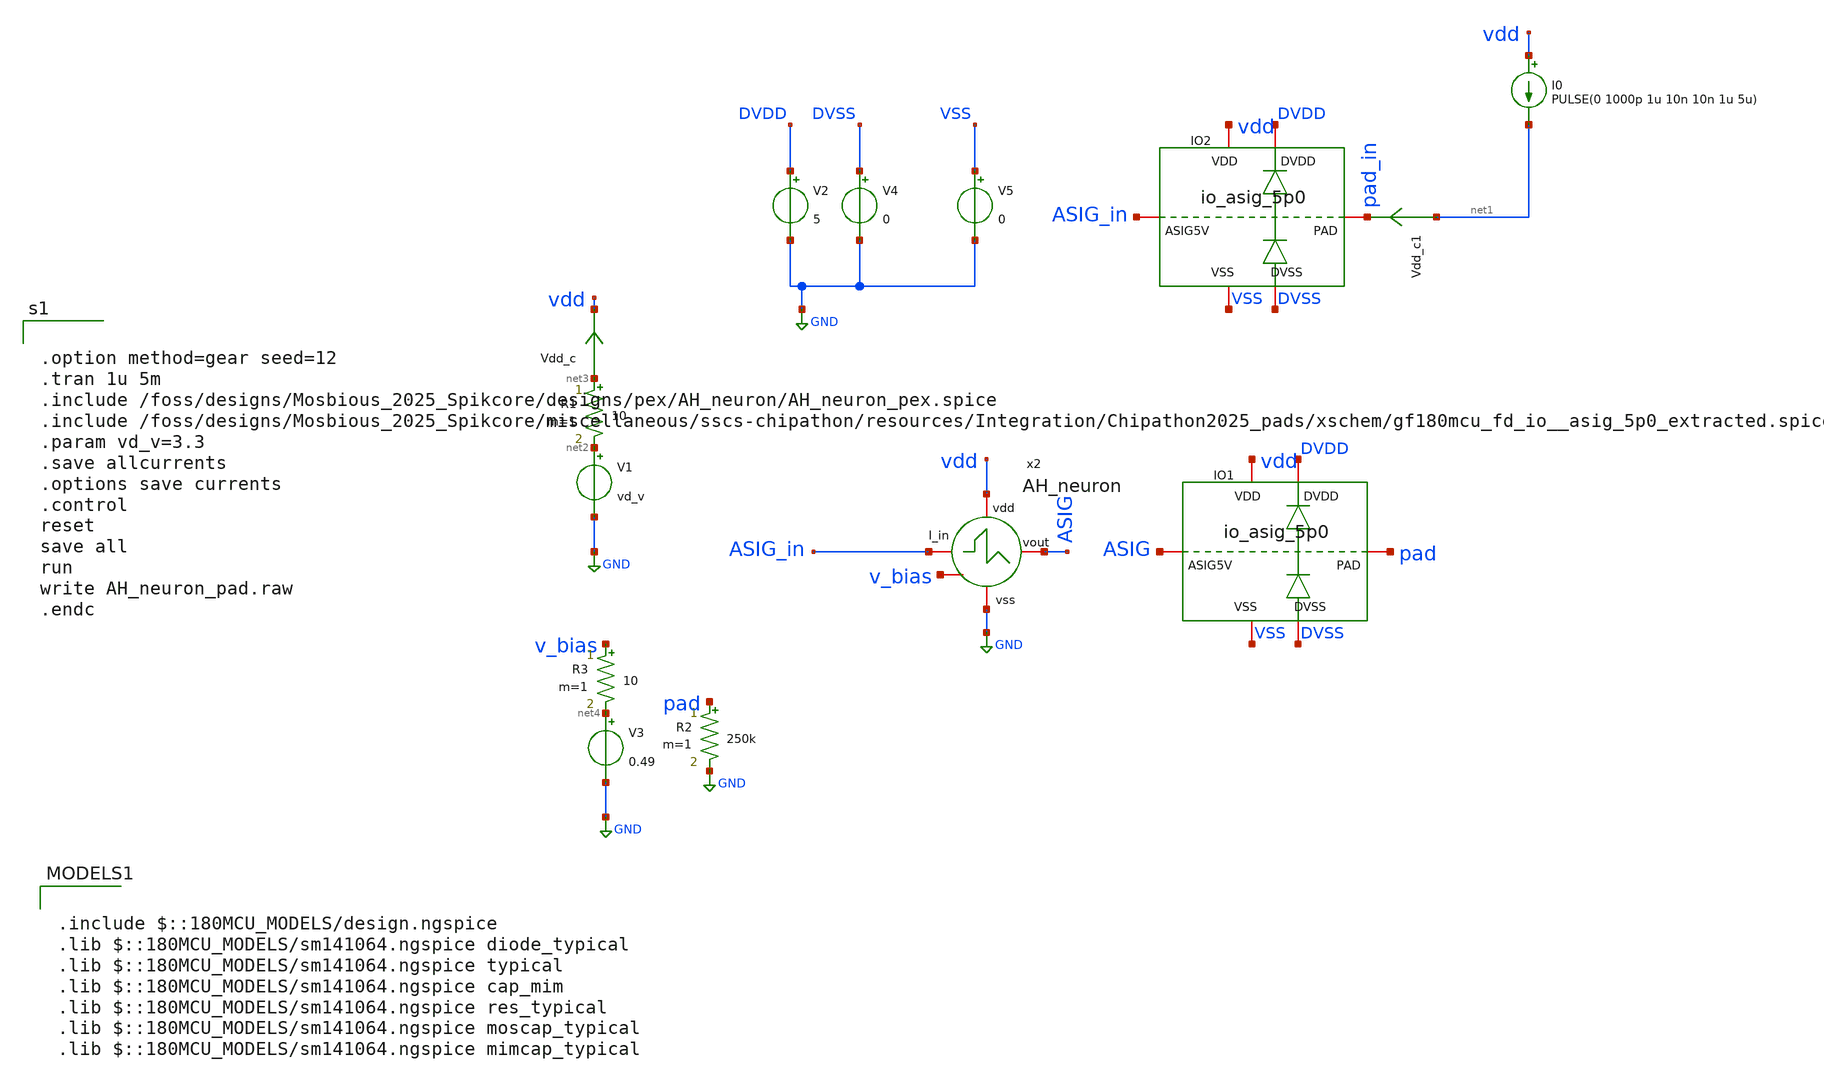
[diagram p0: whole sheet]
** sch_path: designs/libs/tb_core_analogs_pads/tb_AH_neuron/AH_neuron.sch
**.subckt AH_neuron
V1 net2 GND vd_v
Vdd_c net3 vdd 0
.save i(vdd_c)
I0 vdd net1 PULSE(0 1000p 1u 10n 10n 1u 5u)
R1 net3 net2 10 m=1
R2 pad GND 250k m=1
Vdd_c1 net1 pad_in 0
.save i(vdd_c1)
V2 DVDD GND 5
V4 DVSS GND 0
V5 VSS GND 0
XIO1 DVSS DVDD VSS vdd pad ASIG gf180mcu_fd_io__asig_5p0_extracted
V3 net4 GND 0.49
R3 v_bias net4 10 m=1
XIO2 DVSS DVDD VSS vdd pad_in ASIG_in gf180mcu_fd_io__asig_5p0_extracted
x2 vdd ASIG_in ASIG GND v_bias AH_neuron
**** begin user architecture code


.option method=gear seed=12
.tran 1u 5m
.include /foss/designs/Mosbious_2025_Spikcore/designs/pex/AH_neuron/AH_neuron_pex.spice
.include /foss/designs/Mosbious_2025_Spikcore/miscellaneous/sscs-chipathon/resources/Integration/Chipathon2025_pads/xschem/gf180mcu_fd_io__asig_5p0_extracted.spice
.param vd_v=3.3
.save allcurrents
.options save currents
.control
reset
save all
run
write AH_neuron_pad.raw
.endc



.include $::180MCU_MODELS/design.ngspice
.lib $::180MCU_MODELS/sm141064.ngspice diode_typical
.lib $::180MCU_MODELS/sm141064.ngspice typical
.lib $::180MCU_MODELS/sm141064.ngspice cap_mim
.lib $::180MCU_MODELS/sm141064.ngspice res_typical
.lib $::180MCU_MODELS/sm141064.ngspice moscap_typical
.lib $::180MCU_MODELS/sm141064.ngspice mimcap_typical

**** end user architecture code
**.ends
.GLOBAL GND
.end
